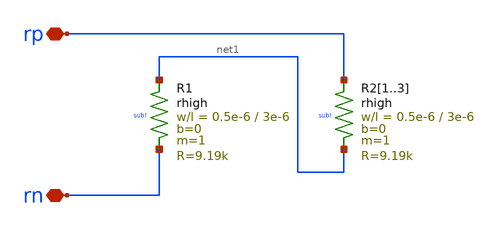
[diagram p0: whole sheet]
** sch_path: xschem/bandgap_banba_res-13k.sch
* (c) 2024 H. Pretl, Apache-2.0 license
**.subckt bandgap_banba_res-13k rp rn
*.iopin rp
*.iopin rn
XR1 net1 rn sub! rhigh w=0.5e-6 l=3e-6 m=1 b=0 mm_ok=1
XR21 rp net1 sub! rhigh w=0.5e-6 l=3e-6 m=1 b=0 mm_ok=1
XR22 rp net1 sub! rhigh w=0.5e-6 l=3e-6 m=1 b=0 mm_ok=1
XR23 rp net1 sub! rhigh w=0.5e-6 l=3e-6 m=1 b=0 mm_ok=1
**.ends
.end
